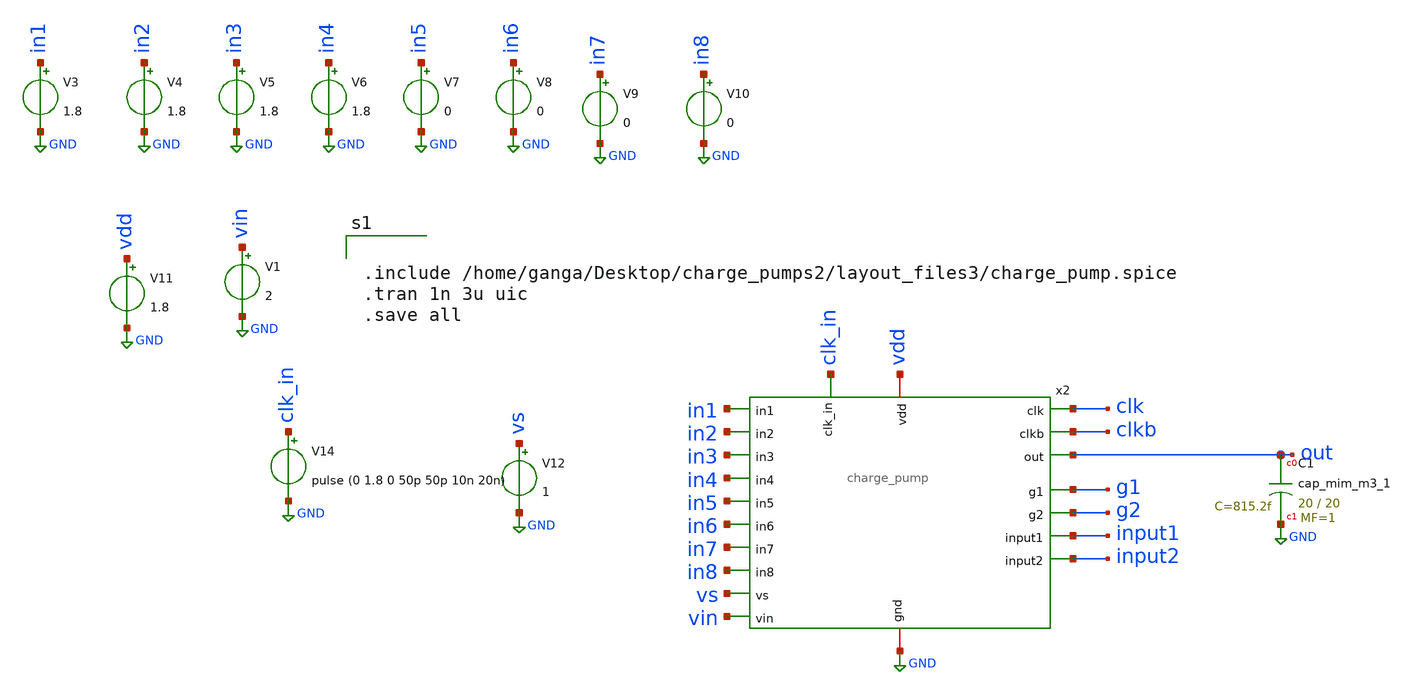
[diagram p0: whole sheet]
** sch_path: xschem/charge_pumps2/CP2_post_layout1.sch
**.subckt CP2_post_layout1
V1 vin GND 2
V3 in1 GND 1.8
V4 in2 GND 1.8
V5 in3 GND 1.8
V6 in4 GND 1.8
V7 in5 GND 0
V8 in6 GND 0
V9 in7 GND 0
V10 in8 GND 0
V11 vdd GND 1.8
V12 vs GND 1
XC1 out GND sky130_fd_pr__cap_mim_m3_1 W=20 L=20 MF=1 m=1
V14 clk_in GND pulse (0 1.8 0 50p 50p 10n 20n)
x2 in8 in7 in6 in5 in4 in3 in2 in1 vdd GND input1 input2 g2 g1 clk clkb vin out clk_in charge_pump
**** begin user architecture code

** opencircuitdesign pdks install
.lib $::SKYWATER_MODELS/sky130.lib.spice tt




.include /home/ganga/Desktop/charge_pumps2/layout_files3/charge_pump.spice
.tran 1n 3u uic
.save all


**** end user architecture code
**.ends
.GLOBAL GND
.end
